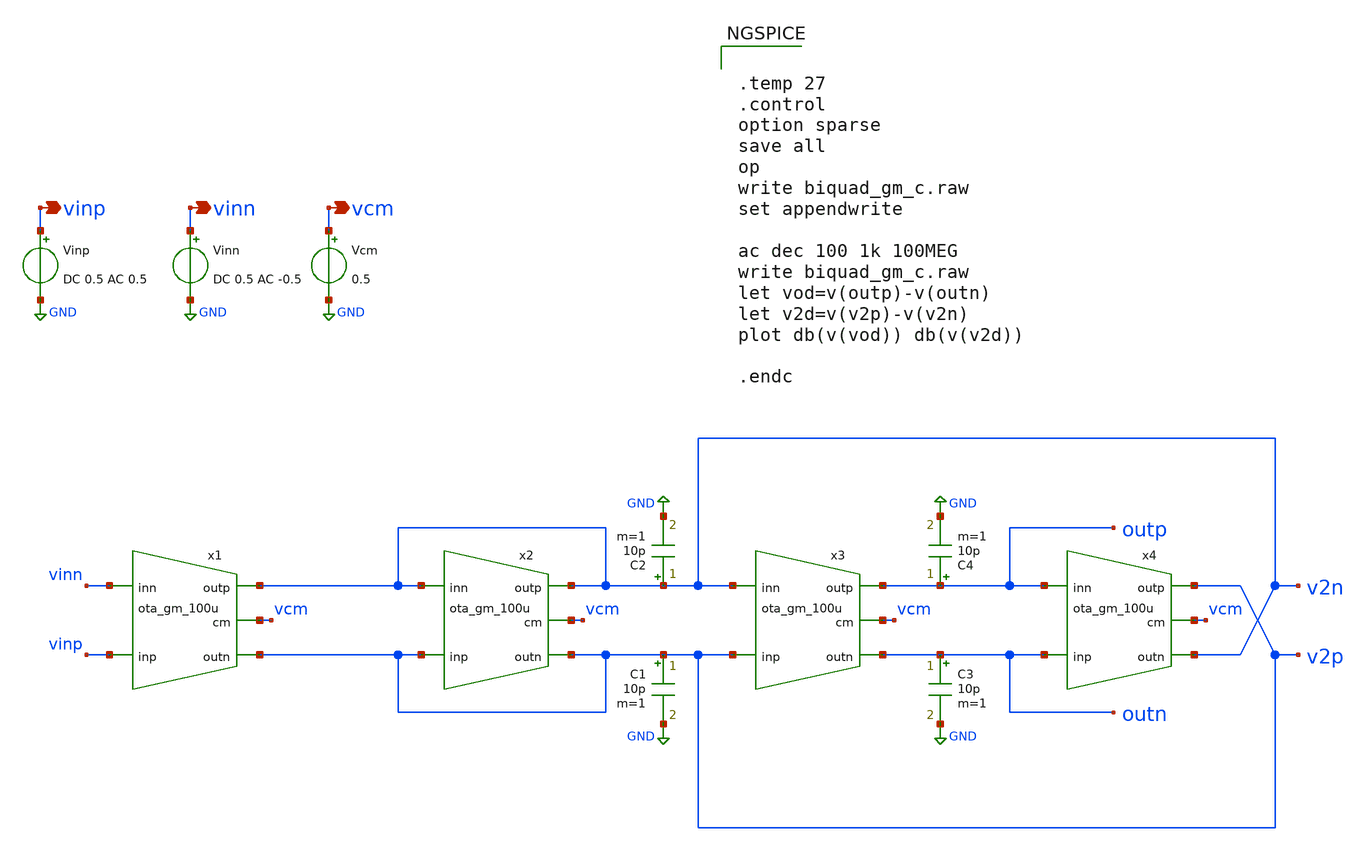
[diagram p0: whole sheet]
** sch_path: prj/template/2_Idealized_circuits/biquad_gm_c_schaum.sch
**.subckt biquad_gm_c_schaum vinp vinn vcm
*.opin vinp
*.opin vinn
*.opin vcm
x1 vinp vinn v2n v2p vcm ota_gm_100u
x2 v2p v2n v2n v2p vcm ota_gm_100u
C1 v2p GND 10p m=1
Vinp vinp GND DC 0.5 AC 0.5
Vinn vinn GND DC 0.5 AC -0.5
Vcm vcm GND 0.5
C2 v2n GND 10p m=1
x3 v2p v2n outp outn vcm ota_gm_100u
x4 outn outp v2p v2n vcm ota_gm_100u
C3 outn GND 10p m=1
C4 outp GND 10p m=1
**** begin user architecture code


.temp 27
.control
option sparse
save all
op
write biquad_gm_c.raw
set appendwrite

ac dec 100 1k 100MEG
write biquad_gm_c.raw
let vod=v(outp)-v(outn)
let v2d=v(v2p)-v(v2n)
plot db(v(vod)) db(v(v2d))

.endc


**** end user architecture code
**.ends
.GLOBAL GND
.end
